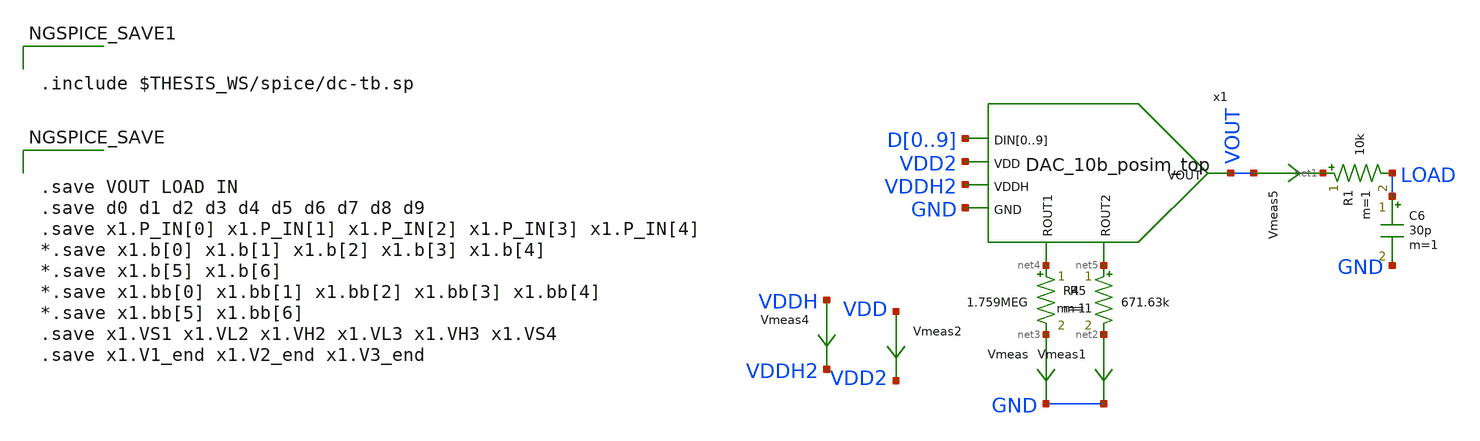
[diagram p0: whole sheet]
** sch_path: xschem/10b_DAC_dc-tb.sch
.lib $::SKYWATER_MODELS/sky130.lib.spice tt
.include $::SKYWATER_STDCELLS/sky130_fd_sc_hd.spice

**.subckt 10b_DAC_dc-tb
C6 LOAD GND 30p m=1
R1 net1 LOAD 10k m=1
Vmeas1 net2 GND 0
.save i(vmeas1)
Vmeas net3 GND 0
.save i(vmeas)
Vmeas2 VDD VDD2 0
.save i(vmeas2)
Vmeas4 VDDH VDDH2 0
.save i(vmeas4)
Vmeas5 VOUT net1 0
.save i(vmeas5)
x1 D0 D1 D2 D3 D4 D5 D6 D7 D8 D9 net4 net5 VDD2 VDDH2 GND VOUT DAC_10b_posim_top
R4 net4 net3 1.759MEG m=1
R5 net5 net2 671.63k m=1
**** begin user architecture code


.save VOUT LOAD IN
.save d0 d1 d2 d3 d4 d5 d6 d7 d8 d9
.save x1.P_IN[0] x1.P_IN[1] x1.P_IN[2] x1.P_IN[3] x1.P_IN[4]
*.save x1.b[0] x1.b[1] x1.b[2] x1.b[3] x1.b[4]
*.save x1.b[5] x1.b[6]
*.save x1.bb[0] x1.bb[1] x1.bb[2] x1.bb[3] x1.bb[4]
*.save x1.bb[5] x1.bb[6]
.save x1.VS1 x1.VL2 x1.VH2 x1.VL3 x1.VH3 x1.VS4
.save x1.V1_end x1.V2_end x1.V3_end




.include $THESIS_WS/spice/dc-tb.sp


**** end user architecture code
**.ends
.end
